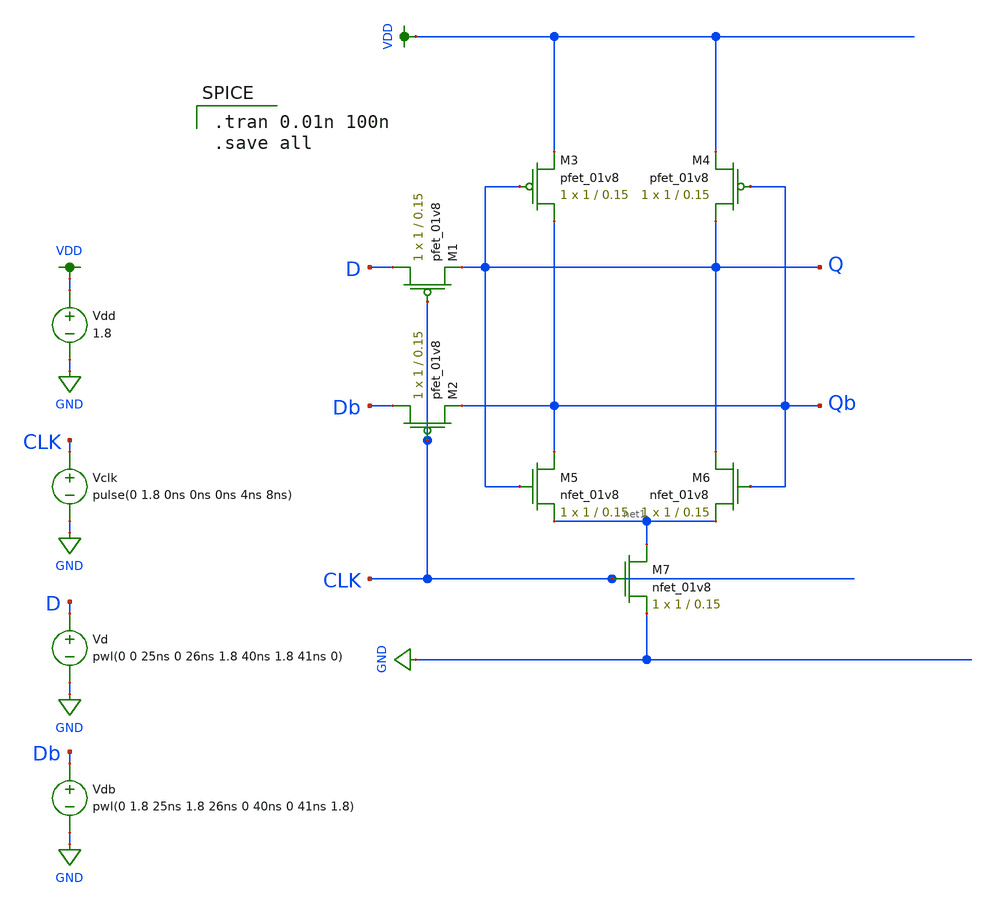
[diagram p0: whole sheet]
** sch_path: simulation/shift_register/andrew_mp2_files/d_flipflop/d_flipflop_single_test_harness.sch
**.subckt d_flipflop_single_test_harness
XM1 D CLK Q VDD sky130_fd_pr__pfet_01v8 L=0.15 W=1 nf=1 ad='int((nf+1)/2) * W/nf * 0.29' as='int((nf+2)/2) * W/nf * 0.29'
+ pd='2*int((nf+1)/2) * (W/nf + 0.29)' ps='2*int((nf+2)/2) * (W/nf + 0.29)' nrd='0.29 / W' nrs='0.29 / W'
+ sa=0 sb=0 sd=0 mult=1 m=1
XM2 Db CLK Qb VDD sky130_fd_pr__pfet_01v8 L=0.15 W=1 nf=1 ad='int((nf+1)/2) * W/nf * 0.29' as='int((nf+2)/2) * W/nf * 0.29'
+ pd='2*int((nf+1)/2) * (W/nf + 0.29)' ps='2*int((nf+2)/2) * (W/nf + 0.29)' nrd='0.29 / W' nrs='0.29 / W'
+ sa=0 sb=0 sd=0 mult=1 m=1
XM3 Qb Q VDD VDD sky130_fd_pr__pfet_01v8 L=0.15 W=1 nf=1 ad='int((nf+1)/2) * W/nf * 0.29' as='int((nf+2)/2) * W/nf * 0.29'
+ pd='2*int((nf+1)/2) * (W/nf + 0.29)' ps='2*int((nf+2)/2) * (W/nf + 0.29)' nrd='0.29 / W' nrs='0.29 / W'
+ sa=0 sb=0 sd=0 mult=1 m=1
XM5 Qb Q net1 GND sky130_fd_pr__nfet_01v8 L=0.15 W=1 nf=1 ad='int((nf+1)/2) * W/nf * 0.29' as='int((nf+2)/2) * W/nf * 0.29'
+ pd='2*int((nf+1)/2) * (W/nf + 0.29)' ps='2*int((nf+2)/2) * (W/nf + 0.29)' nrd='0.29 / W' nrs='0.29 / W'
+ sa=0 sb=0 sd=0 mult=1 m=1
XM7 net1 CLK GND GND sky130_fd_pr__nfet_01v8 L=0.15 W=1 nf=1 ad='int((nf+1)/2) * W/nf * 0.29' as='int((nf+2)/2) * W/nf * 0.29'
+ pd='2*int((nf+1)/2) * (W/nf + 0.29)' ps='2*int((nf+2)/2) * (W/nf + 0.29)' nrd='0.29 / W' nrs='0.29 / W'
+ sa=0 sb=0 sd=0 mult=1 m=1
XM4 Q Qb VDD VDD sky130_fd_pr__pfet_01v8 L=0.15 W=1 nf=1 ad='int((nf+1)/2) * W/nf * 0.29' as='int((nf+2)/2) * W/nf * 0.29'
+ pd='2*int((nf+1)/2) * (W/nf + 0.29)' ps='2*int((nf+2)/2) * (W/nf + 0.29)' nrd='0.29 / W' nrs='0.29 / W'
+ sa=0 sb=0 sd=0 mult=1 m=1
XM6 Q Qb net1 GND sky130_fd_pr__nfet_01v8 L=0.15 W=1 nf=1 ad='int((nf+1)/2) * W/nf * 0.29' as='int((nf+2)/2) * W/nf * 0.29'
+ pd='2*int((nf+1)/2) * (W/nf + 0.29)' ps='2*int((nf+2)/2) * (W/nf + 0.29)' nrd='0.29 / W' nrs='0.29 / W'
+ sa=0 sb=0 sd=0 mult=1 m=1
Vdd VDD GND 1.8
Vclk CLK GND pulse(0 1.8 0ns 0ns 0ns 4ns 8ns)
Vd D GND pwl(0 0 25ns 0 26ns 1.8 40ns 1.8 41ns 0)
Vdb Db GND pwl(0 1.8 25ns 1.8 26ns 0 40ns 0 41ns 1.8)
**** begin user architecture code

.option wnflag=1
.lib ~/skywater/skywater-pdk/libraries/sky130_fd_pr_ngspice/latest/models/sky130.lib.spice tt


.tran 0.01n 100n
.save all

**** end user architecture code
**.ends
.GLOBAL VDD
.GLOBAL GND
.end
